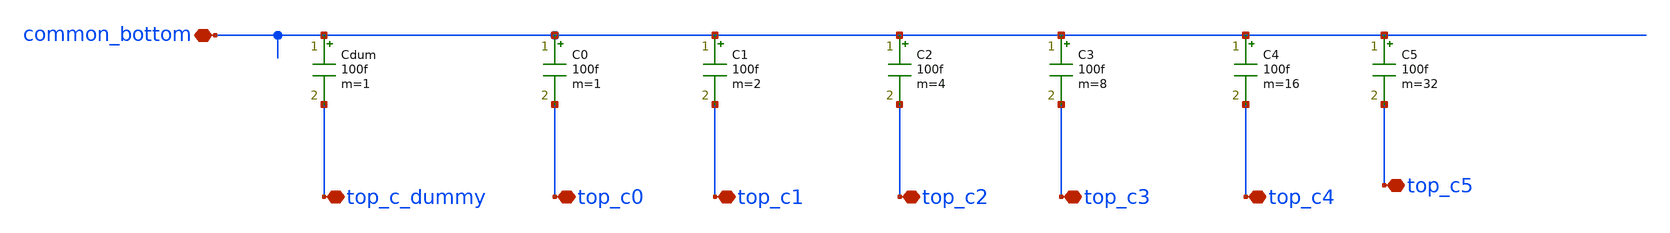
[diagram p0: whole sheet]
** sch_path: maple0705/SAR_ADC/xschem/cap_array_ideal.sch
**.subckt cap_array_ideal common_bottom top_c1 top_c0 top_c_dummy top_c2 top_c4 top_c5 top_c3
*.iopin common_bottom
*.iopin top_c1
*.iopin top_c0
*.iopin top_c_dummy
*.iopin top_c2
*.iopin top_c4
*.iopin top_c5
*.iopin top_c3
Cdum common_bottom top_c_dummy 100f m=1
C0 common_bottom top_c0 100f m=1
C1 common_bottom top_c1 100f m=2
C2 common_bottom top_c2 100f m=4
C3 common_bottom top_c3 100f m=8
C4 common_bottom top_c4 100f m=16
C5 common_bottom top_c5 100f m=32
**.ends
.end
